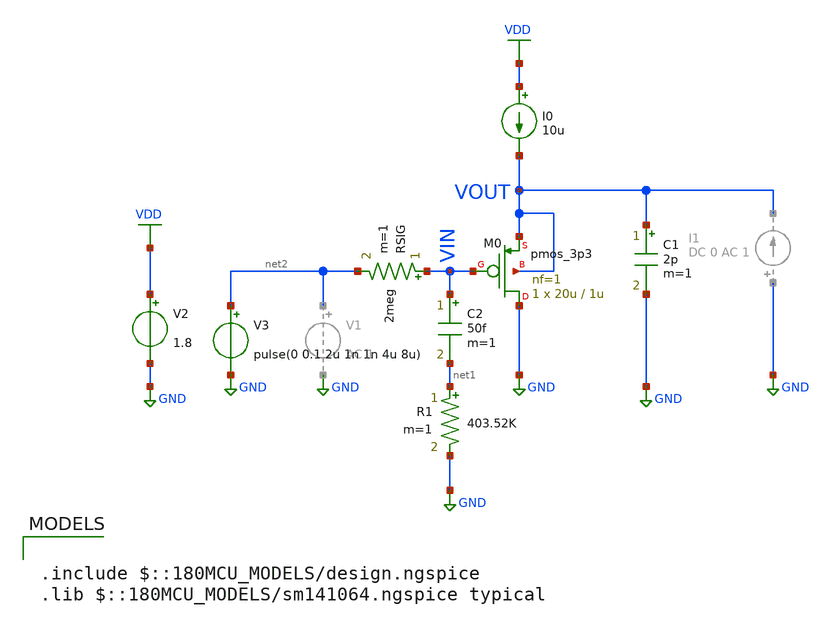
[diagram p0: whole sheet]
** sch_path: ITI_Labs/Lab4/Design/Lab04_compensator.sch
**.subckt Lab04_compensator
I0 VDD VOUT 10u
V2 VDD GND 1.8
RSIG VIN net2 2meg m=1
XM0 GND VIN VOUT VOUT pmos_3p3 L=1u W=20u nf=1 ad='int((nf+1)/2) * W/nf * 0.18u' as='int((nf+2)/2) * W/nf * 0.18u'
+ pd='2*int((nf+1)/2) * (W/nf + 0.18u)' ps='2*int((nf+2)/2) * (W/nf + 0.18u)' nrd='0.18u / W' nrs='0.18u / W'
+ sa=0 sb=0 sd=0 m=1
R1 net1 GND 403.52K m=1
C2 VIN net1 50f m=1
V3 net2 GND pulse(0 0.1 2u 1n 1n 4u 8u)
C1 VOUT GND 2p m=1
**** begin user architecture code

.include $::180MCU_MODELS/design.ngspice
.lib $::180MCU_MODELS/sm141064.ngspice typical



.include sim_script_Comepnsator.sim

**** end user architecture code
**.ends
.GLOBAL GND
.GLOBAL VDD
.end
